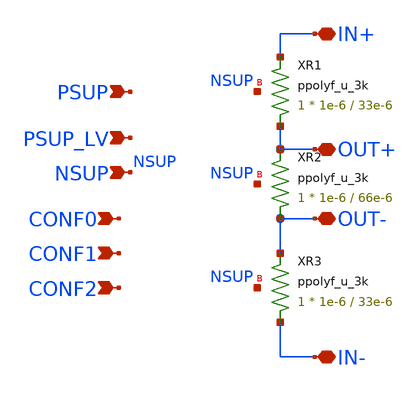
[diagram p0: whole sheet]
** sch_path: xschem/blocks/rdiv_0_84_12db/rdiv_0_84_12db.sch
**.subckt rdiv_0_84_12db IN+ IN- OUT- OUT+ PSUP PSUP_LV NSUP CONF0 CONF1 CONF2
*.iopin IN+
*.iopin IN-
*.iopin OUT-
*.iopin OUT+
*.ipin PSUP
*.ipin PSUP_LV
*.ipin NSUP
*.ipin CONF0
*.ipin CONF1
*.ipin CONF2
XR1 OUT+ IN+ NSUP ppolyf_u_3k r_width=1e-6 r_length=33e-6 m=1
XR2 OUT- OUT+ NSUP ppolyf_u_3k r_width=1e-6 r_length=66e-6 m=1
XR3 IN- OUT- NSUP ppolyf_u_3k r_width=1e-6 r_length=33e-6 m=1
**.ends
.end
